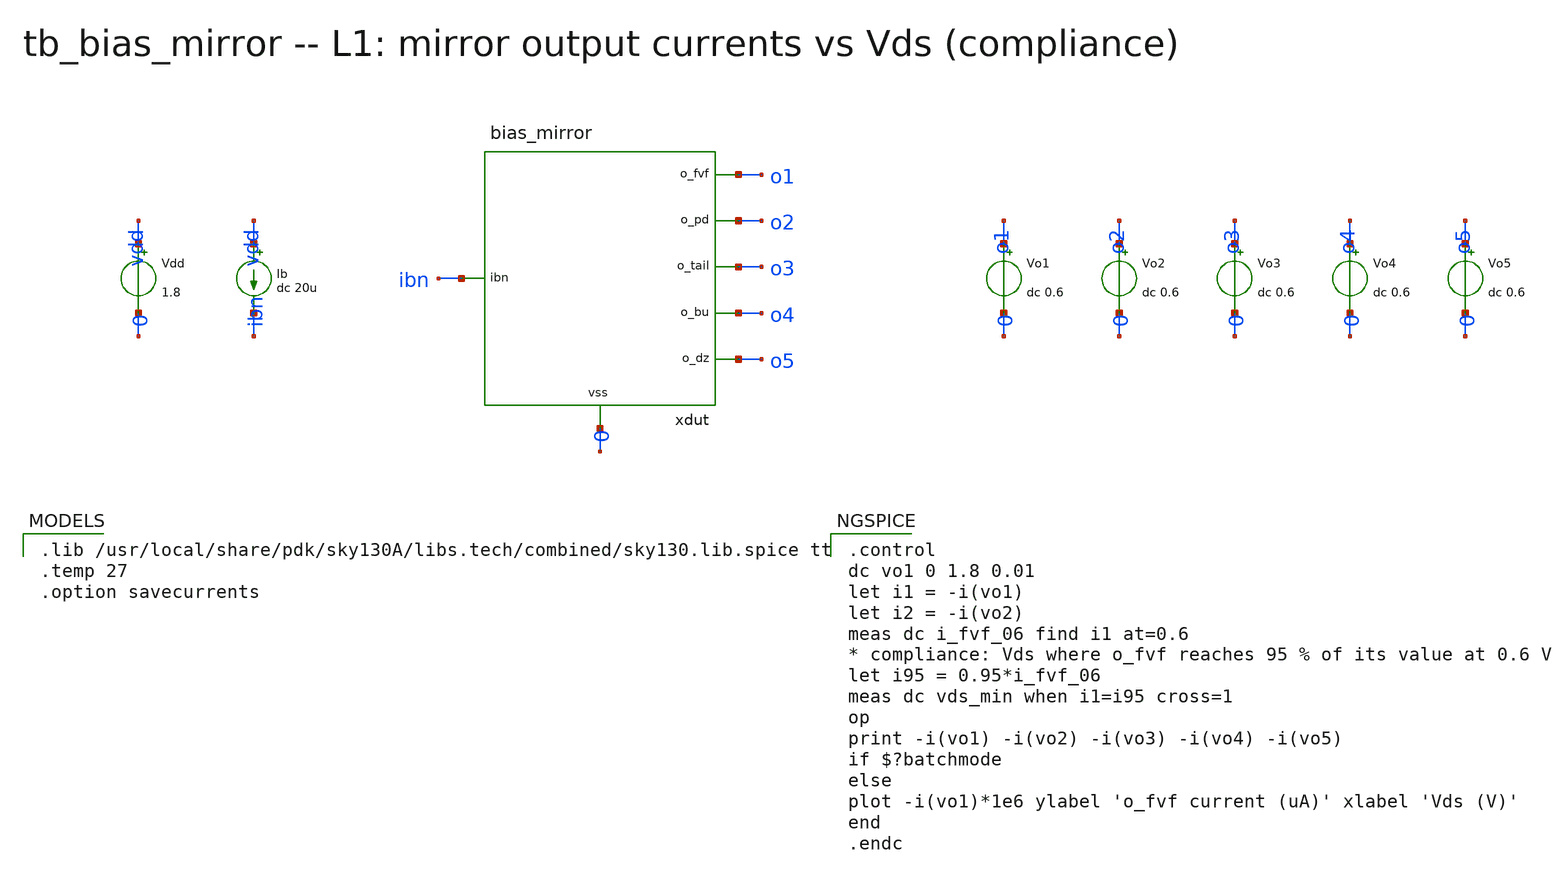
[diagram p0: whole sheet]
** sch_path: xschem/onetops_tb/tb_bias_mirror.sch
**.subckt tb_bias_mirror
Vdd vdd 0 1.8
Ib vdd ibn dc 20u
xdut ibn o1 o2 o3 o4 o5 0 bias_mirror
Vo1 o1 0 dc 0.6
Vo2 o2 0 dc 0.6
Vo3 o3 0 dc 0.6
Vo4 o4 0 dc 0.6
Vo5 o5 0 dc 0.6
**** begin user architecture code

.lib /usr/local/share/pdk/sky130A/libs.tech/combined/sky130.lib.spice tt
.temp 27
.option savecurrents


.control
dc vo1 0 1.8 0.01
let i1 = -i(vo1)
let i2 = -i(vo2)
meas dc i_fvf_06 find i1 at=0.6
* compliance: Vds where o_fvf reaches 95 % of its value at 0.6 V
let i95 = 0.95*i_fvf_06
meas dc vds_min when i1=i95 cross=1
op
print -i(vo1) -i(vo2) -i(vo3) -i(vo4) -i(vo5)
if $?batchmode
else
plot -i(vo1)*1e6 ylabel 'o_fvf current (uA)' xlabel 'Vds (V)'
end
.endc

**** end user architecture code
**.ends

* expanding   symbol:  onetops/bias_mirror.sym # of pins=7
** sym_path: xschem/onetops/bias_mirror.sym
** sch_path: xschem/onetops/bias_mirror.sch
.subckt bias_mirror ibn o_fvf o_pd o_tail o_bu o_dz vss
*.ipin ibn
*.opin o_fvf
*.opin o_pd
*.opin o_tail
*.opin o_bu
*.opin o_dz
*.iopin vss
XMN0 ibn ibn vss vss sky130_fd_pr__nfet_01v8 L=1 W=4 nf=1 ad='int((1 + 1)/2) * 4 / 1 * 0.29' as='int((1 + 2)/2) * 4 / 1 * 0.29'
+ pd='2*int((1 + 1)/2) * (4 / 1 + 0.29)' ps='2*int((1 + 2)/2) * (4 / 1 + 0.29)' nrd='0.29 / 4 ' nrs='0.29 / 4 '
+ sa=0 sb=0 sd=0 mult=1 m=1
XMN1 o_fvf ibn vss vss sky130_fd_pr__nfet_01v8 L=1 W=1 nf=1 ad='int((1 + 1)/2) * 1 / 1 * 0.29' as='int((1 + 2)/2) * 1 / 1 * 0.29'
+ pd='2*int((1 + 1)/2) * (1 / 1 + 0.29)' ps='2*int((1 + 2)/2) * (1 / 1 + 0.29)' nrd='0.29 / 1 ' nrs='0.29 / 1 '
+ sa=0 sb=0 sd=0 mult=1 m=1
XMN2 o_bu ibn vss vss sky130_fd_pr__nfet_01v8 L=1 W=4 nf=1 ad='int((1 + 1)/2) * 4 / 1 * 0.29' as='int((1 + 2)/2) * 4 / 1 * 0.29'
+ pd='2*int((1 + 1)/2) * (4 / 1 + 0.29)' ps='2*int((1 + 2)/2) * (4 / 1 + 0.29)' nrd='0.29 / 4 ' nrs='0.29 / 4 '
+ sa=0 sb=0 sd=0 mult=1 m=1
XMN3 o_pd ibn vss vss sky130_fd_pr__nfet_01v8 L=1 W=1 nf=1 ad='int((1 + 1)/2) * 1 / 1 * 0.29' as='int((1 + 2)/2) * 1 / 1 * 0.29'
+ pd='2*int((1 + 1)/2) * (1 / 1 + 0.29)' ps='2*int((1 + 2)/2) * (1 / 1 + 0.29)' nrd='0.29 / 1 ' nrs='0.29 / 1 '
+ sa=0 sb=0 sd=0 mult=1 m=1
XMN4 o_tail ibn vss vss sky130_fd_pr__nfet_01v8 L=1 W=4 nf=1 ad='int((1 + 1)/2) * 4 / 1 * 0.29' as='int((1 + 2)/2) * 4 / 1 * 0.29'
+ pd='2*int((1 + 1)/2) * (4 / 1 + 0.29)' ps='2*int((1 + 2)/2) * (4 / 1 + 0.29)' nrd='0.29 / 4 ' nrs='0.29 / 4 '
+ sa=0 sb=0 sd=0 mult=2 m=2
XMN5 o_dz ibn vss vss sky130_fd_pr__nfet_01v8 L=1 W=4 nf=1 ad='int((1 + 1)/2) * 4 / 1 * 0.29' as='int((1 + 2)/2) * 4 / 1 * 0.29'
+ pd='2*int((1 + 1)/2) * (4 / 1 + 0.29)' ps='2*int((1 + 2)/2) * (4 / 1 + 0.29)' nrd='0.29 / 4 ' nrs='0.29 / 4 '
+ sa=0 sb=0 sd=0 mult=1 m=1
.ends

.end
